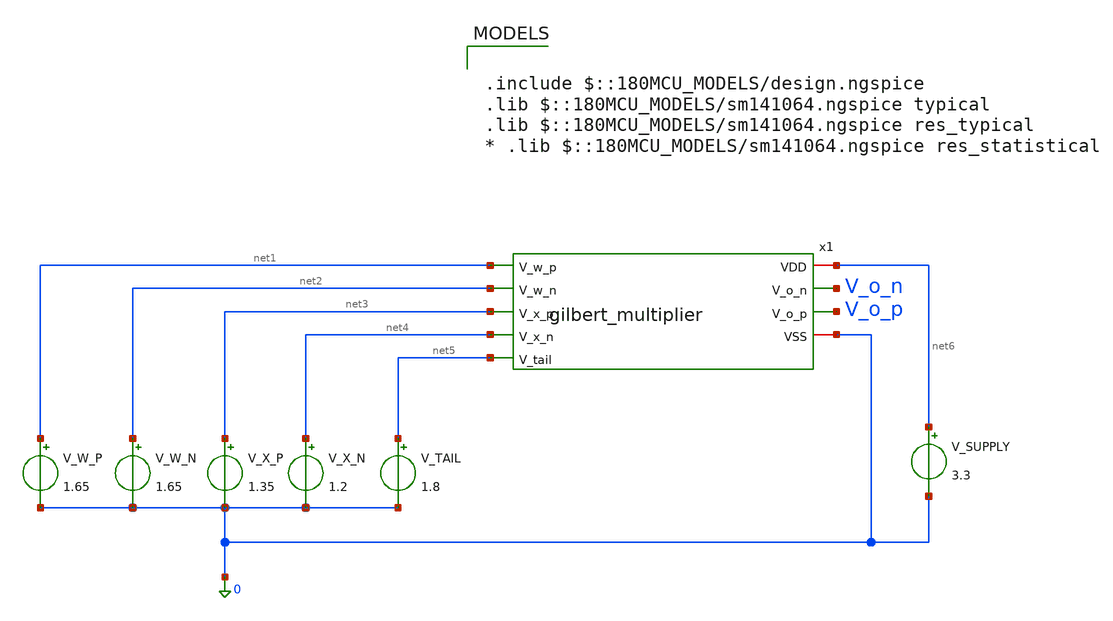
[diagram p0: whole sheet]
** sch_path: schematics/tb_gilbert_multiplier.sch
**.subckt tb_gilbert_multiplier
x1 net6 V_o_n V_o_p net1 net2 net3 net4 net5 0 gilbert_multiplier
V_X_P net3 0 1.35
V_X_N net4 0 1.2
V_TAIL net5 0 1.8
V_W_P net1 0 1.65
V_W_N net2 0 1.65
V_SUPPLY net6 0 3.3
**** begin user architecture code


.control
  * Nested Sweep:
  * 1. Sweep Weight (V_W_P) from 1.15V to 2.15V in 10mV steps.
  * 2. Step Sensor (V_X_P) from 1.10V to 1.30V in 50mV steps.
  dc V_W_P 1.15 2.15 0.01 V_X_P 1.10 1.30 0.05

  * Calculate differential output
  let V_diff_out = v(V_o_p) - v(V_o_n)

  * Export the family of curves to a text file
  wrdata /foss/designs/analog-perceptron-gf180mcu/schematics/sweep_4quadrant.txt V_diff_out

  * Plot the result in the Xschem GUI
  plot V_diff_out
.endc



.include $::180MCU_MODELS/design.ngspice
.lib $::180MCU_MODELS/sm141064.ngspice typical
.lib $::180MCU_MODELS/sm141064.ngspice res_typical
* .lib $::180MCU_MODELS/sm141064.ngspice res_statistical

**** end user architecture code
**.ends
.end
